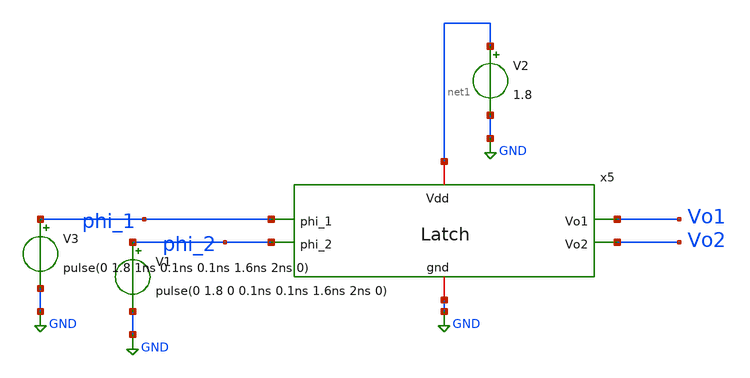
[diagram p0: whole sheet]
** sch_path: xschem/latch_tb.sch
**.subckt latch_tb
x1 net1 phi_1 Vo1 Vo2 phi_2 GND latch
V1 phi_2 GND pulse(0 1.8 0 0.1ns 0.1ns 1.6ns 2ns 0)
V2 net1 GND 1.8
V3 phi_1 GND pulse(0 1.8 1ns 0.1ns 0.1ns 1.6ns 2ns 0)
**** begin user architecture code



.lib /usr/local/share/pdk/sky130A/libs.tech/ngspice/sky130.lib.spice tt

.control
        tran 0.01n 10ns
        plot v(phi_1) v(phi_2) v(Vo1) v(Vo2)
.endc
.save all



**** end user architecture code
**.ends

* expanding   symbol:  latch.sym # of pins=6
** sym_path: xschem/latch.sym
** sch_path: xschem/latch.sch
.subckt latch Vdd phi_1 Vo1 Vo2 phi_2 gnd
*.ipin phi_1
*.ipin phi_2
*.iopin Vdd
*.iopin gnd
*.opin Vo1
*.opin Vo2
XM1 Vo2 phi_1 Vdd Vdd sky130_fd_pr__pfet_01v8 L=0.15 W=30 nf=1 ad='int((nf+1)/2) * W/nf * 0.29' as='int((nf+2)/2) * W/nf * 0.29'
+ pd='2*int((nf+1)/2) * (W/nf + 0.29)' ps='2*int((nf+2)/2) * (W/nf + 0.29)' nrd='0.29 / W' nrs='0.29 / W'
+ sa=0 sb=0 sd=0 mult=1 m=1
XM2 Vo1 phi_2 Vdd Vdd sky130_fd_pr__pfet_01v8 L=0.15 W=30 nf=1 ad='int((nf+1)/2) * W/nf * 0.29' as='int((nf+2)/2) * W/nf * 0.29'
+ pd='2*int((nf+1)/2) * (W/nf + 0.29)' ps='2*int((nf+2)/2) * (W/nf + 0.29)' nrd='0.29 / W' nrs='0.29 / W'
+ sa=0 sb=0 sd=0 mult=1 m=1
XM3 Vo1 Vo2 Vdd Vdd sky130_fd_pr__pfet_01v8 L=0.15 W=10 nf=1 ad='int((nf+1)/2) * W/nf * 0.29' as='int((nf+2)/2) * W/nf * 0.29'
+ pd='2*int((nf+1)/2) * (W/nf + 0.29)' ps='2*int((nf+2)/2) * (W/nf + 0.29)' nrd='0.29 / W' nrs='0.29 / W'
+ sa=0 sb=0 sd=0 mult=1 m=1
XM4 Vo2 Vo1 Vdd Vdd sky130_fd_pr__pfet_01v8 L=0.15 W=10 nf=1 ad='int((nf+1)/2) * W/nf * 0.29' as='int((nf+2)/2) * W/nf * 0.29'
+ pd='2*int((nf+1)/2) * (W/nf + 0.29)' ps='2*int((nf+2)/2) * (W/nf + 0.29)' nrd='0.29 / W' nrs='0.29 / W'
+ sa=0 sb=0 sd=0 mult=1 m=1
XM5 Vo1 Vo2 net1 gnd sky130_fd_pr__nfet_01v8 L=0.15 W=5 nf=1 ad='int((nf+1)/2) * W/nf * 0.29' as='int((nf+2)/2) * W/nf * 0.29'
+ pd='2*int((nf+1)/2) * (W/nf + 0.29)' ps='2*int((nf+2)/2) * (W/nf + 0.29)' nrd='0.29 / W' nrs='0.29 / W'
+ sa=0 sb=0 sd=0 mult=1 m=1
XM6 net1 phi_1 gnd gnd sky130_fd_pr__nfet_01v8 L=0.15 W=15 nf=1 ad='int((nf+1)/2) * W/nf * 0.29' as='int((nf+2)/2) * W/nf * 0.29'
+ pd='2*int((nf+1)/2) * (W/nf + 0.29)' ps='2*int((nf+2)/2) * (W/nf + 0.29)' nrd='0.29 / W' nrs='0.29 / W'
+ sa=0 sb=0 sd=0 mult=1 m=1
XM7 Vo2 Vo1 net2 gnd sky130_fd_pr__nfet_01v8 L=0.15 W=5 nf=1 ad='int((nf+1)/2) * W/nf * 0.29' as='int((nf+2)/2) * W/nf * 0.29'
+ pd='2*int((nf+1)/2) * (W/nf + 0.29)' ps='2*int((nf+2)/2) * (W/nf + 0.29)' nrd='0.29 / W' nrs='0.29 / W'
+ sa=0 sb=0 sd=0 mult=1 m=1
XM8 net2 phi_2 gnd gnd sky130_fd_pr__nfet_01v8 L=0.15 W=15 nf=1 ad='int((nf+1)/2) * W/nf * 0.29' as='int((nf+2)/2) * W/nf * 0.29'
+ pd='2*int((nf+1)/2) * (W/nf + 0.29)' ps='2*int((nf+2)/2) * (W/nf + 0.29)' nrd='0.29 / W' nrs='0.29 / W'
+ sa=0 sb=0 sd=0 mult=1 m=1
.ends

.GLOBAL GND
.end
